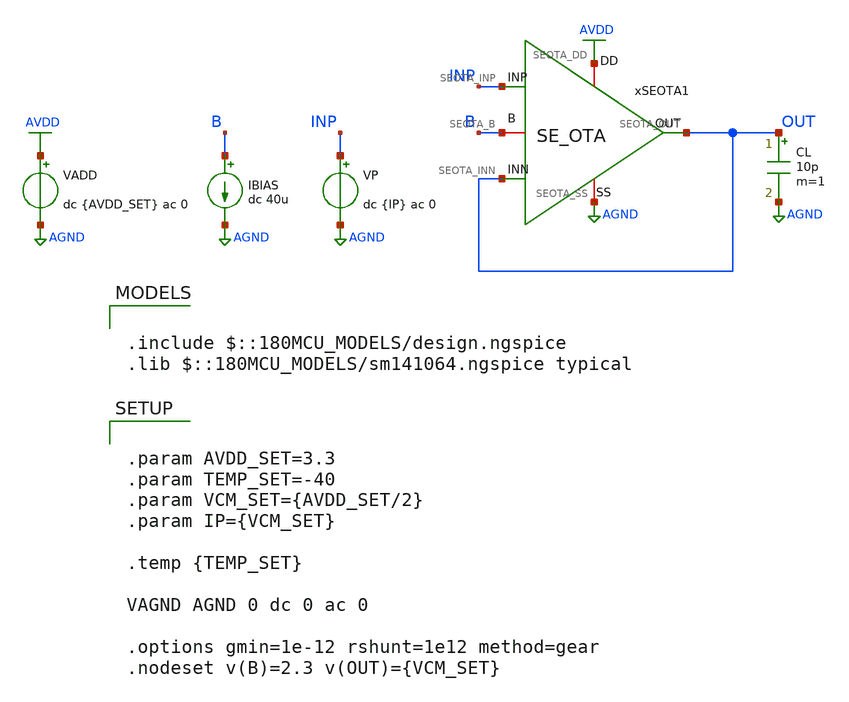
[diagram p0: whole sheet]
** sch_path: Design_Files/IC Design/Testbench/SE_OTA_OTA/Close_Loop/SE_OTA_TB_CL_Cn40.sch
**.subckt SE_OTA_TB_CL_Cn40
IBIAS B AGND dc 40u
VADD AVDD AGND dc {AVDD_SET} ac 0
.save i(vadd)
CL OUT AGND 10p m=1
VP INP AGND dc {IP} ac 0
xSEOTA1 AVDD AGND INP OUT OUT B SE_OTA
**** begin user architecture code

.include $::180MCU_MODELS/design.ngspice
.lib $::180MCU_MODELS/sm141064.ngspice typical



.control
destroy all
save all
set wr_singlescale

shell mkdir -p /foss/designs/ECG_Acquisition_IC/Measurement_Results/IC_Simulation/SE_OTA

let avdd_run = 3.3
let vcm_run  = avdd_run/2

* OP
alter @VP[DC] = $&vcm_run
alter @VP[ACMAG] = 0
alter @VADD[ACMAG] = 0
alter @VAGND[ACMAG] = 0

op
let cl_avdd  = v(AVDD)
let cl_inp   = v(INP)
let cl_out   = v(OUT)
let cl_b     = v(B)
let cl_idd   = -vadd#branch
let cl_ibias = 40e-6
wrdata /foss/designs/ECG_Acquisition_IC/Measurement_Results/IC_Simulation/SE_OTA/Cn40.cl_op.txt
+ cl_avdd cl_inp cl_out cl_b cl_idd cl_ibias

* Swing
dc VP 0 $&avdd_run 0.001
let sw_inp = v(INP)
let sw_out = v(OUT)
let sw_idd = -vadd#branch
wrdata /foss/designs/ECG_Acquisition_IC/Measurement_Results/IC_Simulation/SE_OTA/Cn40.cl_swing.txt
+ sw_inp sw_out sw_idd

* Slew
alter @VP[PULSE] = [ 1.0 2.0 1u 1n 1n 10u 20u 0 ]

tran 1n 30u
wrdata /foss/designs/ECG_Acquisition_IC/Measurement_Results/IC_Simulation/SE_OTA/Cn40.cl_slew.txt
+ v(INP) v(OUT)

.endc




.param AVDD_SET=3.3
.param TEMP_SET=-40
.param VCM_SET={AVDD_SET/2}
.param IP={VCM_SET}

.temp {TEMP_SET}

VAGND AGND 0 dc 0 ac 0

.options gmin=1e-12 rshunt=1e12 method=gear
.nodeset v(B)=2.3 v(OUT)={VCM_SET}


**** end user architecture code
**.ends

* expanding   symbol:  ECG_Acquisition_IC/Design_Files/IC Design/Schematic/SE_OTA/SE_OTA.sym # of
*+ pins=6
** sym_path: Design_Files/IC Design/Schematic/SE_OTA/SE_OTA.sym
** sch_path: Design_Files/IC Design/Schematic/SE_OTA/SE_OTA.sch
.subckt SE_OTA SEOTA_DD SEOTA_SS SEOTA_INP SEOTA_INN SEOTA_OUT SEOTA_B
*.iopin SEOTA_DD
*.iopin SEOTA_SS
*.ipin SEOTA_INP
*.ipin SEOTA_INN
*.opin SEOTA_OUT
*.iopin SEOTA_B
XM3 net4 net4 SEOTA_DD SEOTA_DD pfet_03v3 L=4u W=1u nf=1 ad='int((nf+1)/2) * W/nf * 0.18u' as='int((nf+2)/2) * W/nf * 0.18u'
+ pd='2*int((nf+1)/2) * (W/nf + 0.18u)' ps='2*int((nf+2)/2) * (W/nf + 0.18u)' nrd='0.18u / W' nrs='0.18u / W'
+ sa=0 sb=0 sd=0 m=60
XM7 SEOTA_OUT SEOTA_B SEOTA_SS SEOTA_SS nfet_03v3 L=0.5u W=1u nf=1 ad='int((nf+1)/2) * W/nf * 0.18u'
+ as='int((nf+2)/2) * W/nf * 0.18u' pd='2*int((nf+1)/2) * (W/nf + 0.18u)' ps='2*int((nf+2)/2) * (W/nf + 0.18u)'
+ nrd='0.18u / W' nrs='0.18u / W' sa=0 sb=0 sd=0 m=100
Rz net1 net2 3.8k m=1
XM5 net3 SEOTA_B SEOTA_SS SEOTA_SS nfet_03v3 L=2u W=1u nf=1 ad='int((nf+1)/2) * W/nf * 0.18u' as='int((nf+2)/2) * W/nf * 0.18u'
+ pd='2*int((nf+1)/2) * (W/nf + 0.18u)' ps='2*int((nf+2)/2) * (W/nf + 0.18u)' nrd='0.18u / W' nrs='0.18u / W'
+ sa=0 sb=0 sd=0 m=10
XM6 SEOTA_OUT net1 SEOTA_DD SEOTA_DD pfet_03v3 L=0.5u W=1u nf=1 ad='int((nf+1)/2) * W/nf * 0.18u' as='int((nf+2)/2) * W/nf * 0.18u'
+ pd='2*int((nf+1)/2) * (W/nf + 0.18u)' ps='2*int((nf+2)/2) * (W/nf + 0.18u)' nrd='0.18u / W' nrs='0.18u / W'
+ sa=0 sb=0 sd=0 m=400
XM8 SEOTA_B SEOTA_B SEOTA_SS SEOTA_SS nfet_03v3 L=2u W=1u nf=1 ad='int((nf+1)/2) * W/nf * 0.18u' as='int((nf+2)/2) * W/nf * 0.18u'
+ pd='2*int((nf+1)/2) * (W/nf + 0.18u)' ps='2*int((nf+2)/2) * (W/nf + 0.18u)' nrd='0.18u / W' nrs='0.18u / W'
+ sa=0 sb=0 sd=0 m=20
Cc net2 SEOTA_OUT 2p m=1
XM4 net1 net4 SEOTA_DD SEOTA_DD pfet_03v3 L=4u W=1u nf=1 ad='int((nf+1)/2) * W/nf * 0.18u' as='int((nf+2)/2) * W/nf * 0.18u'
+ pd='2*int((nf+1)/2) * (W/nf + 0.18u)' ps='2*int((nf+2)/2) * (W/nf + 0.18u)' nrd='0.18u / W' nrs='0.18u / W'
+ sa=0 sb=0 sd=0 m=60
XM1 net4 SEOTA_INN net3 SEOTA_SS nfet_03v3 L=4u W=1u nf=1 ad='int((nf+1)/2) * W/nf * 0.18u' as='int((nf+2)/2) * W/nf * 0.18u'
+ pd='2*int((nf+1)/2) * (W/nf + 0.18u)' ps='2*int((nf+2)/2) * (W/nf + 0.18u)' nrd='0.18u / W' nrs='0.18u / W'
+ sa=0 sb=0 sd=0 m=400
XM2 net1 SEOTA_INP net3 SEOTA_SS nfet_03v3 L=4u W=1u nf=1 ad='int((nf+1)/2) * W/nf * 0.18u' as='int((nf+2)/2) * W/nf * 0.18u'
+ pd='2*int((nf+1)/2) * (W/nf + 0.18u)' ps='2*int((nf+2)/2) * (W/nf + 0.18u)' nrd='0.18u / W' nrs='0.18u / W'
+ sa=0 sb=0 sd=0 m=400
.ends

.GLOBAL AVDD
.GLOBAL AGND
.end
